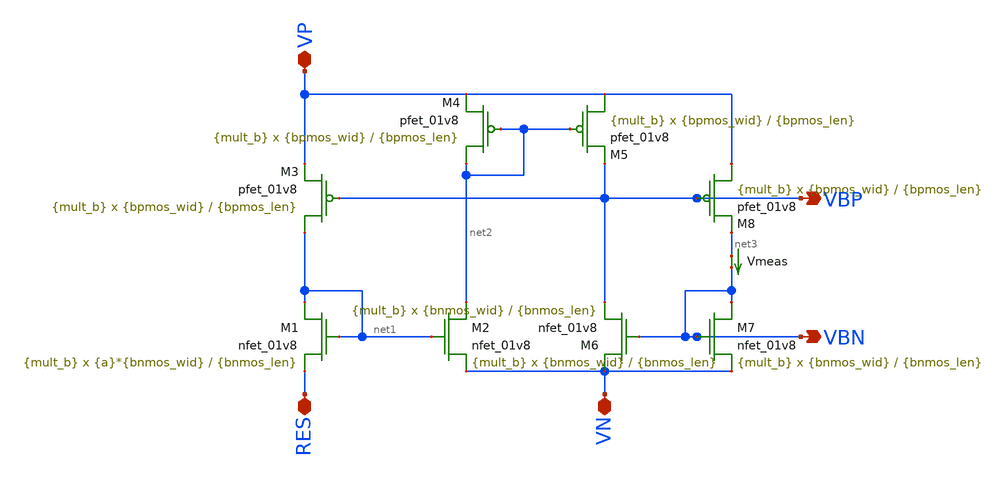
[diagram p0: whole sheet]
** sch_path: bbg.sch
**.subckt bbg VP VN RES VBP VBN
*.iopin VP
*.iopin VN
*.iopin RES
*.opin VBP
*.opin VBN
XM1 net1 net1 RES VN sky130_fd_pr__nfet_01v8 L={bnmos_len} W={a}*{bnmos_wid} nf=1 ad='int((nf+1)/2) * W/nf * 0.29'
+ as='int((nf+2)/2) * W/nf * 0.29' pd='2*int((nf+1)/2) * (W/nf + 0.29)' ps='2*int((nf+2)/2) * (W/nf + 0.29)'
+ nrd='0.29 / W' nrs='0.29 / W' sa=0 sb=0 sd=0 mult={mult_b} m={mult_b}
XM2 net2 net1 VN VN sky130_fd_pr__nfet_01v8 L={bnmos_len} W={bnmos_wid} nf=1 ad='int((nf+1)/2) * W/nf * 0.29'
+ as='int((nf+2)/2) * W/nf * 0.29' pd='2*int((nf+1)/2) * (W/nf + 0.29)' ps='2*int((nf+2)/2) * (W/nf + 0.29)'
+ nrd='0.29 / W' nrs='0.29 / W' sa=0 sb=0 sd=0 mult={mult_b} m={mult_b}
XM3 net1 VBP VP VP sky130_fd_pr__pfet_01v8 L={bpmos_len} W={bpmos_wid} nf=1 ad='int((nf+1)/2) * W/nf * 0.29'
+ as='int((nf+2)/2) * W/nf * 0.29' pd='2*int((nf+1)/2) * (W/nf + 0.29)' ps='2*int((nf+2)/2) * (W/nf + 0.29)'
+ nrd='0.29 / W' nrs='0.29 / W' sa=0 sb=0 sd=0 mult={mult_b} m={mult_b}
Vmeas net3 VBN 0
.save i(vmeas)
XM6 VN VBN VBP VN sky130_fd_pr__nfet_01v8 L={bnmos_len} W={bnmos_wid} nf=1 ad='int((nf+1)/2) * W/nf * 0.29'
+ as='int((nf+2)/2) * W/nf * 0.29' pd='2*int((nf+1)/2) * (W/nf + 0.29)' ps='2*int((nf+2)/2) * (W/nf + 0.29)'
+ nrd='0.29 / W' nrs='0.29 / W' sa=0 sb=0 sd=0 mult={mult_b} m={mult_b}
XM7 VBN VBN VN VN sky130_fd_pr__nfet_01v8 L={bnmos_len} W={bnmos_wid} nf=1 ad='int((nf+1)/2) * W/nf * 0.29'
+ as='int((nf+2)/2) * W/nf * 0.29' pd='2*int((nf+1)/2) * (W/nf + 0.29)' ps='2*int((nf+2)/2) * (W/nf + 0.29)'
+ nrd='0.29 / W' nrs='0.29 / W' sa=0 sb=0 sd=0 mult={mult_b} m={mult_b}
XM4 net2 net2 VP VP sky130_fd_pr__pfet_01v8 L={bpmos_len} W={bpmos_wid} nf=1 ad='int((nf+1)/2) * W/nf * 0.29'
+ as='int((nf+2)/2) * W/nf * 0.29' pd='2*int((nf+1)/2) * (W/nf + 0.29)' ps='2*int((nf+2)/2) * (W/nf + 0.29)'
+ nrd='0.29 / W' nrs='0.29 / W' sa=0 sb=0 sd=0 mult={mult_b} m={mult_b}
XM5 VP net2 VBP VP sky130_fd_pr__pfet_01v8 L={bpmos_len} W={bpmos_wid} nf=1 ad='int((nf+1)/2) * W/nf * 0.29'
+ as='int((nf+2)/2) * W/nf * 0.29' pd='2*int((nf+1)/2) * (W/nf + 0.29)' ps='2*int((nf+2)/2) * (W/nf + 0.29)'
+ nrd='0.29 / W' nrs='0.29 / W' sa=0 sb=0 sd=0 mult={mult_b} m={mult_b}
XM8 VP VBP net3 VP sky130_fd_pr__pfet_01v8 L={bpmos_len} W={bpmos_wid} nf=1 ad='int((nf+1)/2) * W/nf * 0.29'
+ as='int((nf+2)/2) * W/nf * 0.29' pd='2*int((nf+1)/2) * (W/nf + 0.29)' ps='2*int((nf+2)/2) * (W/nf + 0.29)'
+ nrd='0.29 / W' nrs='0.29 / W' sa=0 sb=0 sd=0 mult={mult_b} m={mult_b}
**.ends
.end
